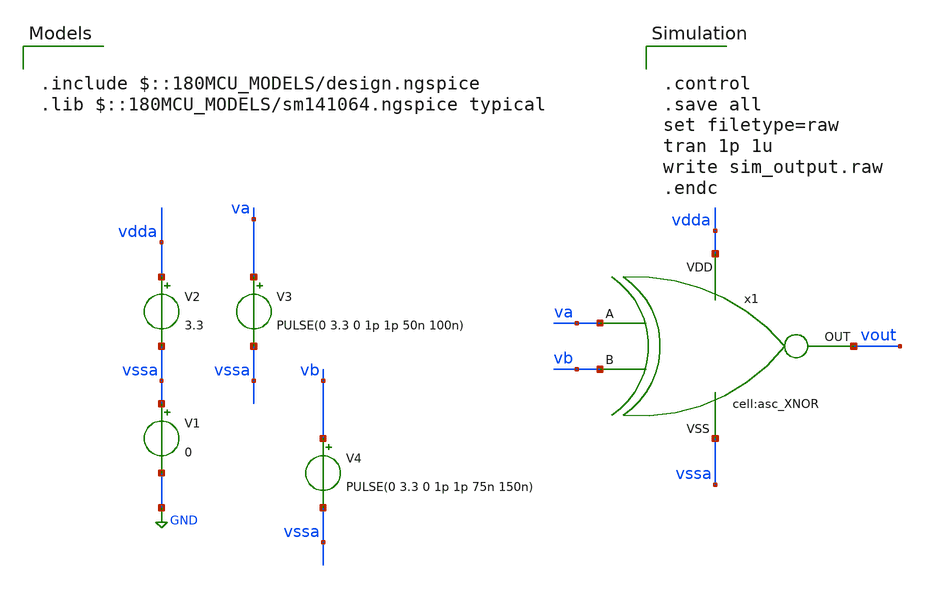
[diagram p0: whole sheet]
** sch_path: designs/libs/xp_tb_analog/tb_asc_XNOR/tb_asc_XNOR.sch
**.subckt tb_asc_XNOR
V1 vssa GND 0
V2 vdda vssa 3.3
V3 va vssa PULSE(0 3.3 0 1p 1p 50n 100n)
V4 vb vssa PULSE(0 3.3 0 1p 1p 75n 150n)
x1 vdda vssa vout va vb asc_XNOR
**** begin user architecture code

.include $::180MCU_MODELS/design.ngspice
.lib $::180MCU_MODELS/sm141064.ngspice typical



.control
.save all
set filetype=raw
tran 1p 1u
write sim_output.raw
.endc


**** end user architecture code
**.ends
.GLOBAL GND
.end
